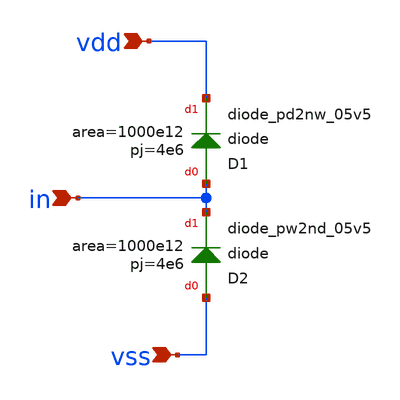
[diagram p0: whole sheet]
** sch_path: IO-cells/xschem/SigPad.sch
**.subckt SigPad in vdd vss
*.ipin in
*.ipin vdd
*.ipin vss
XD1 in vdd sky130_fd_pr__diode_pd2nw_05v5 area=1000e12 pj=4e6
XD2 vss in sky130_fd_pr__diode_pw2nd_05v5 area=1000e12 pj=4e6
**.ends
.end
